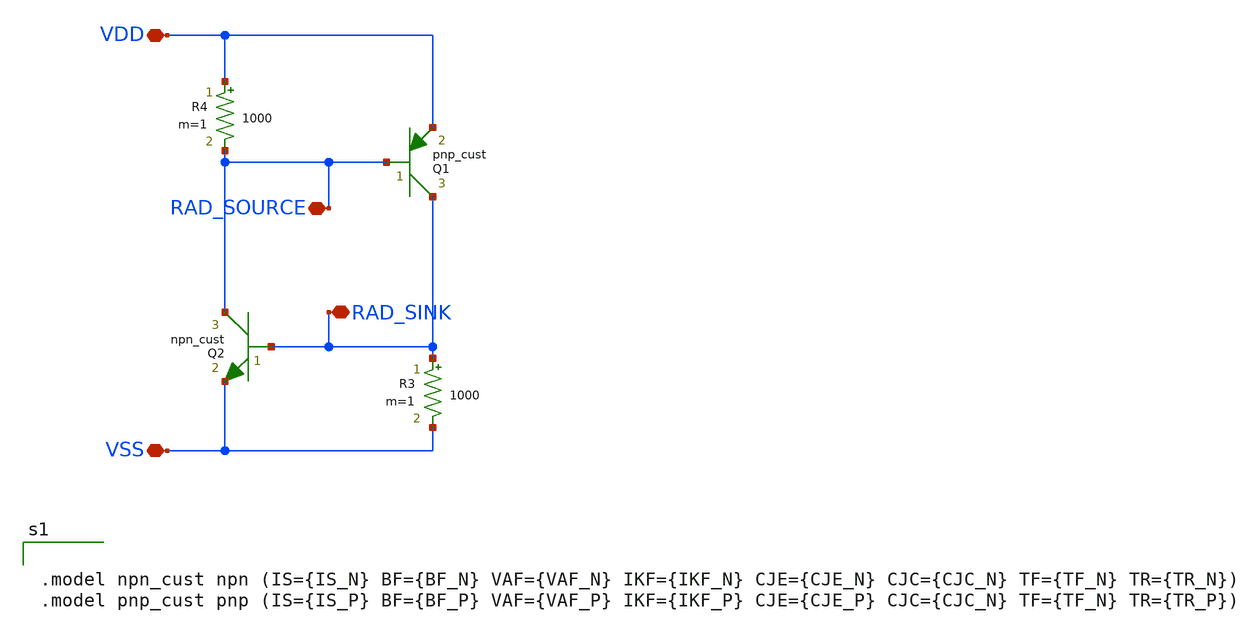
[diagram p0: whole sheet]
** sch_path: latchup/basic_model.sch
**.subckt basic_model VDD VSS RAD_SOURCE RAD_SINK
*.iopin VDD
*.iopin VSS
*.iopin RAD_SOURCE
*.iopin RAD_SINK
Q1 RAD_SINK RAD_SOURCE VDD pnp_cust area=1 m=1
Q2 RAD_SOURCE RAD_SINK VSS npn_cust area=1 m=1
R3 RAD_SINK VSS 1000 m=1
R4 VDD RAD_SOURCE 1000 m=1
**** begin user architecture code


.model npn_cust npn (IS={IS_N} BF={BF_N} VAF={VAF_N} IKF={IKF_N} CJE={CJE_N} CJC={CJC_N} TF={TF_N} TR={TR_N})
.model pnp_cust pnp (IS={IS_P} BF={BF_P} VAF={VAF_P} IKF={IKF_P} CJE={CJE_P} CJC={CJC_N} TF={TF_N} TR={TR_P})


**** end user architecture code
**.ends
.end
